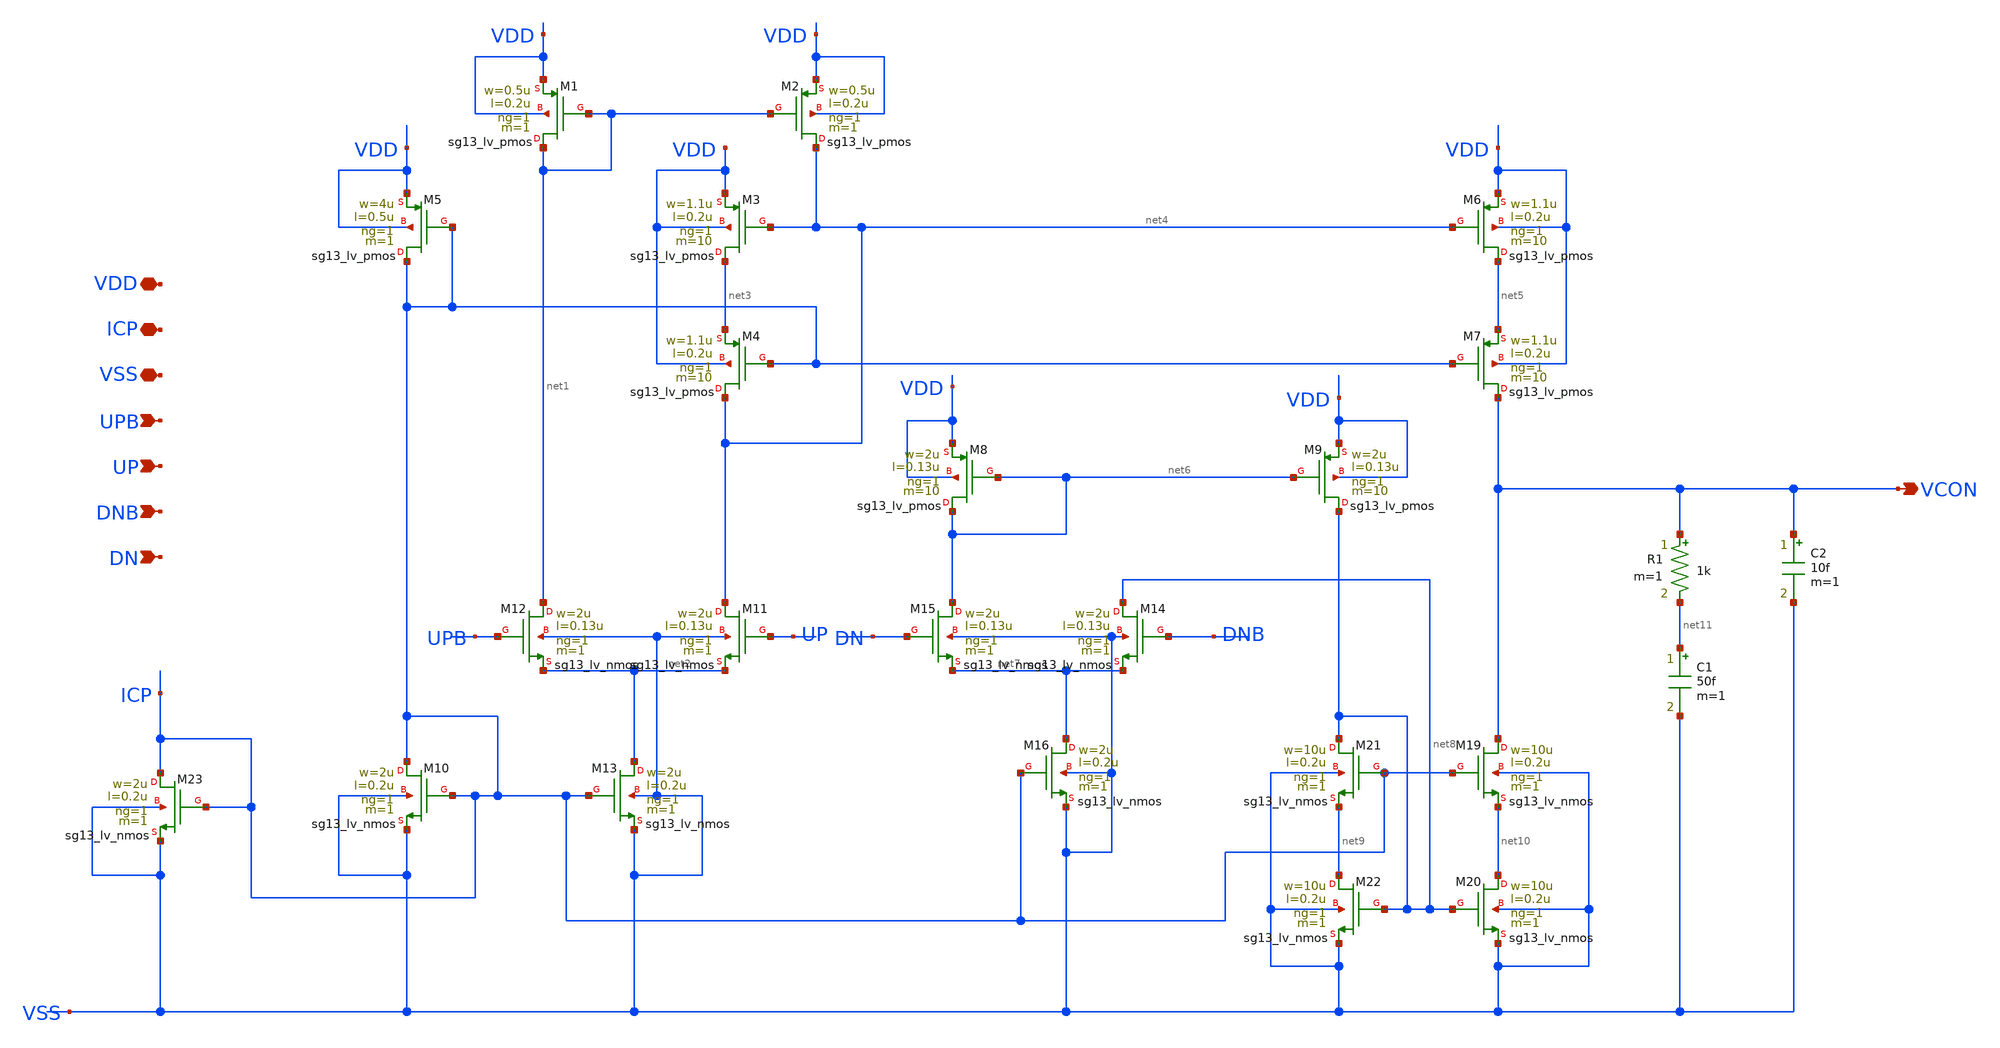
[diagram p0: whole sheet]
** sch_path: Team Designs/Team 1 Design/design_data/xschem/CP_LF/CP_LF.sch
**.subckt CP_LF VDD ICP VSS UPB UP DNB DN VCON
*.iopin VDD
*.iopin ICP
*.iopin VSS
*.ipin UPB
*.ipin UP
*.ipin DNB
*.ipin DN
*.opin VCON
XM1 net1 net1 VDD VDD sg13_lv_pmos w=0.5u l=0.2u ng=1 m=1 mm_ok=1
XM2 net4 net1 VDD VDD sg13_lv_pmos w=0.5u l=0.2u ng=1 m=1 mm_ok=1
XM3 net3 net4 VDD VDD sg13_lv_pmos w=1.1u l=0.2u ng=1 m=10 mm_ok=1
XM4 net4 ICP net3 VDD sg13_lv_pmos w=1.1u l=0.2u ng=1 m=10 mm_ok=1
XM5 ICP ICP VDD VDD sg13_lv_pmos w=4u l=0.5u ng=1 m=1 mm_ok=1
XM6 net5 net4 VDD VDD sg13_lv_pmos w=1.1u l=0.2u ng=1 m=10 mm_ok=1
XM7 VCON ICP net5 VDD sg13_lv_pmos w=1.1u l=0.2u ng=1 m=10 mm_ok=1
XM8 net6 net6 VDD VDD sg13_lv_pmos w=2u l=0.13u ng=1 m=10 mm_ok=1
XM9 net8 net6 VDD VDD sg13_lv_pmos w=2u l=0.13u ng=1 m=10 mm_ok=1
XM10 ICP ICP VSS VSS sg13_lv_nmos w=2u l=0.2u ng=1 m=1 mm_ok=1
XM11 net4 UP net2 VSS sg13_lv_nmos w=2u l=0.13u ng=1 m=1 mm_ok=1
XM12 net1 UPB net2 VSS sg13_lv_nmos w=2u l=0.13u ng=1 m=1 mm_ok=1
XM13 net2 ICP VSS VSS sg13_lv_nmos w=2u l=0.2u ng=1 m=1 mm_ok=1
XM14 net8 DNB net7 VSS sg13_lv_nmos w=2u l=0.13u ng=1 m=1 mm_ok=1
XM15 net6 DN net7 VSS sg13_lv_nmos w=2u l=0.13u ng=1 m=1 mm_ok=1
XM16 net7 ICP VSS VSS sg13_lv_nmos w=2u l=0.2u ng=1 m=1 mm_ok=1
XM19 VCON ICP net10 VSS sg13_lv_nmos w=10u l=0.2u ng=1 m=1 mm_ok=1
XM20 net10 net8 VSS VSS sg13_lv_nmos w=10u l=0.2u ng=1 m=1 mm_ok=1
XM21 net8 ICP net9 VSS sg13_lv_nmos w=10u l=0.2u ng=1 m=1 mm_ok=1
XM22 net9 net8 VSS VSS sg13_lv_nmos w=10u l=0.2u ng=1 m=1 mm_ok=1
R1 VCON net11 1k m=1
C1 net11 VSS 50f m=1
C2 VCON VSS 10f m=1
XM23 ICP ICP VSS VSS sg13_lv_nmos w=2u l=0.2u ng=1 m=1 mm_ok=1
**.ends
.end
